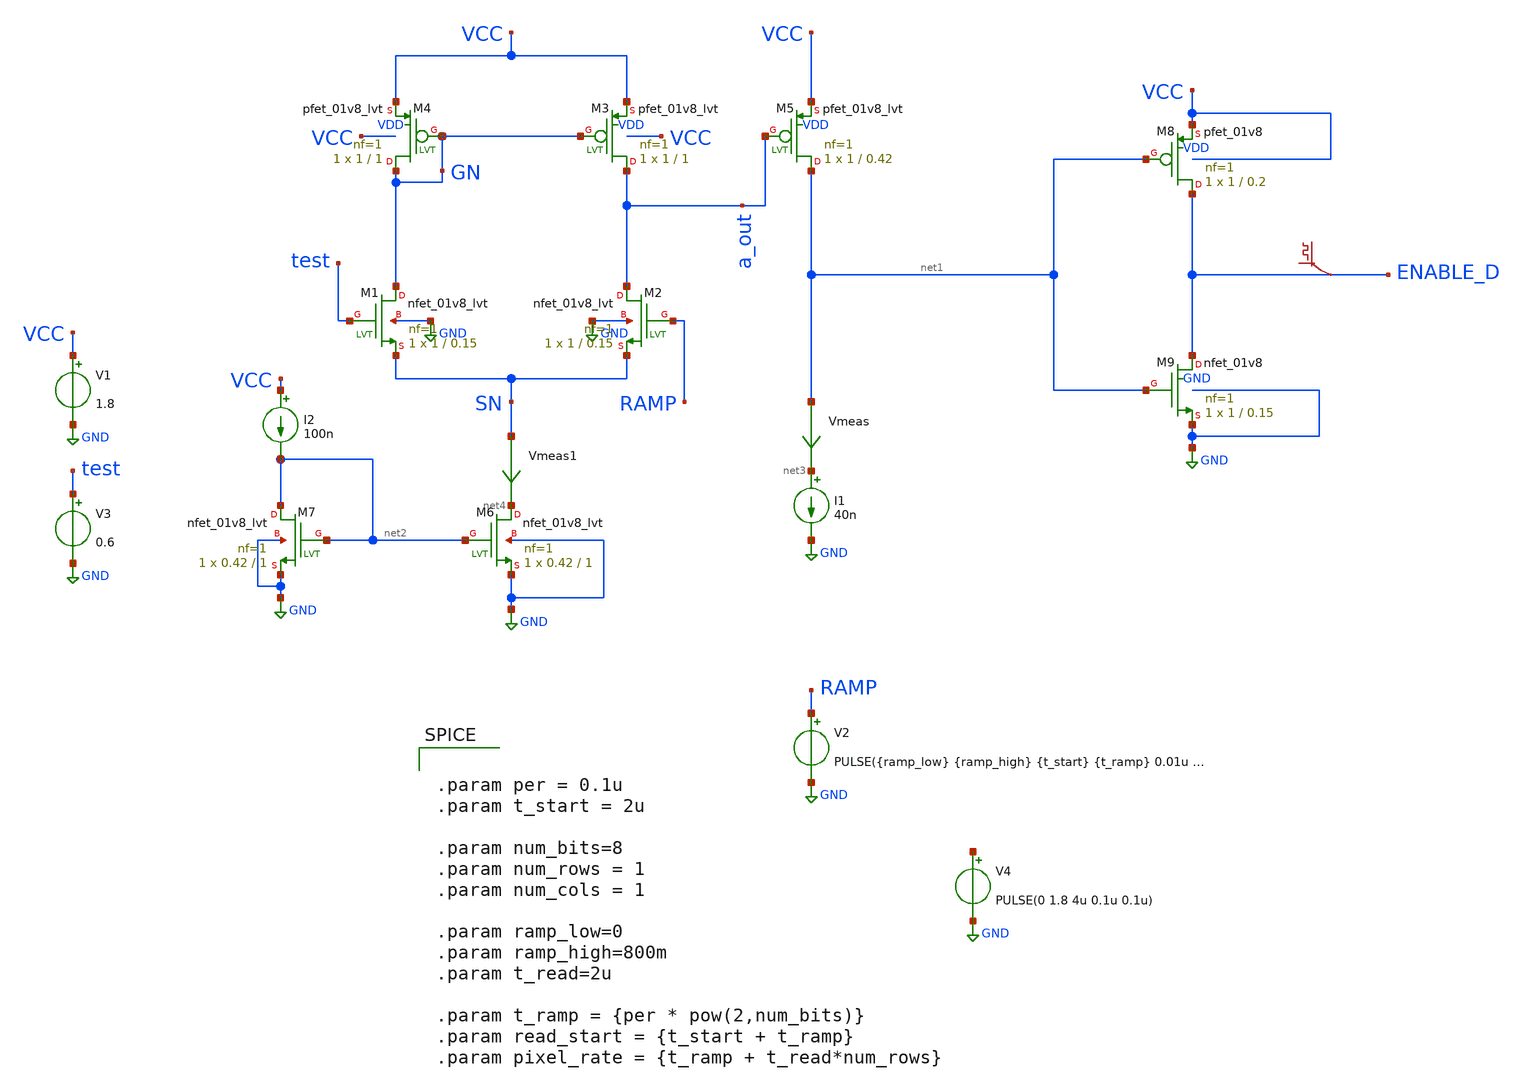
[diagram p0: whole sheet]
** sch_path: xschem/testbench/comp_test.sch
**.subckt comp_test
V1 VCC GND 1.8
V3 test GND 0.6
XM1 GN test SN GND sky130_fd_pr__nfet_01v8_lvt L=0.15 W=1 nf=1 ad='int((nf+1)/2) * W/nf * 0.29' as='int((nf+2)/2) * W/nf * 0.29'
+ pd='2*int((nf+1)/2) * (W/nf + 0.29)' ps='2*int((nf+2)/2) * (W/nf + 0.29)' nrd='0.29 / W' nrs='0.29 / W'
+ sa=0 sb=0 sd=0 mult=1 m=1
XM2 a_out RAMP SN GND sky130_fd_pr__nfet_01v8_lvt L=0.15 W=1 nf=1 ad='int((nf+1)/2) * W/nf * 0.29' as='int((nf+2)/2) * W/nf * 0.29'
+ pd='2*int((nf+1)/2) * (W/nf + 0.29)' ps='2*int((nf+2)/2) * (W/nf + 0.29)' nrd='0.29 / W' nrs='0.29 / W'
+ sa=0 sb=0 sd=0 mult=1 m=1
XM3 a_out GN VCC VDD sky130_fd_pr__pfet_01v8_lvt L=1 W=1 nf=1 ad='int((nf+1)/2) * W/nf * 0.29' as='int((nf+2)/2) * W/nf * 0.29'
+ pd='2*int((nf+1)/2) * (W/nf + 0.29)' ps='2*int((nf+2)/2) * (W/nf + 0.29)' nrd='0.29 / W' nrs='0.29 / W'
+ sa=0 sb=0 sd=0 mult=1 m=1
XM4 GN GN VCC VDD sky130_fd_pr__pfet_01v8_lvt L=1 W=1 nf=1 ad='int((nf+1)/2) * W/nf * 0.29' as='int((nf+2)/2) * W/nf * 0.29'
+ pd='2*int((nf+1)/2) * (W/nf + 0.29)' ps='2*int((nf+2)/2) * (W/nf + 0.29)' nrd='0.29 / W' nrs='0.29 / W'
+ sa=0 sb=0 sd=0 mult=1 m=1
XM5 net1 a_out VCC VDD sky130_fd_pr__pfet_01v8_lvt L=0.42 W=1 nf=1 ad='int((nf+1)/2) * W/nf * 0.29' as='int((nf+2)/2) * W/nf * 0.29'
+ pd='2*int((nf+1)/2) * (W/nf + 0.29)' ps='2*int((nf+2)/2) * (W/nf + 0.29)' nrd='0.29 / W' nrs='0.29 / W'
+ sa=0 sb=0 sd=0 mult=1 m=1
I1 net3 GND 40n
XM8 ENABLE_D net1 VCC VDD sky130_fd_pr__pfet_01v8 L=0.2 W=1 nf=1 ad='int((nf+1)/2) * W/nf * 0.29' as='int((nf+2)/2) * W/nf * 0.29'
+ pd='2*int((nf+1)/2) * (W/nf + 0.29)' ps='2*int((nf+2)/2) * (W/nf + 0.29)' nrd='0.29 / W' nrs='0.29 / W'
+ sa=0 sb=0 sd=0 mult=1 m=1
XM9 ENABLE_D net1 GND GND sky130_fd_pr__nfet_01v8 L=0.15 W=1 nf=1 ad='int((nf+1)/2) * W/nf * 0.29' as='int((nf+2)/2) * W/nf * 0.29'
+ pd='2*int((nf+1)/2) * (W/nf + 0.29)' ps='2*int((nf+2)/2) * (W/nf + 0.29)' nrd='0.29 / W' nrs='0.29 / W'
+ sa=0 sb=0 sd=0 mult=1 m=1
.save v(enable_d)
Vmeas net1 net3 0
.save i(vmeas)
Vmeas1 SN net4 0
.save i(vmeas1)
XM6 net4 net2 GND GND sky130_fd_pr__nfet_01v8_lvt L=1 W=0.42 nf=1 ad='int((nf+1)/2) * W/nf * 0.29' as='int((nf+2)/2) * W/nf * 0.29'
+ pd='2*int((nf+1)/2) * (W/nf + 0.29)' ps='2*int((nf+2)/2) * (W/nf + 0.29)' nrd='0.29 / W' nrs='0.29 / W'
+ sa=0 sb=0 sd=0 mult=1 m=1
XM7 net2 net2 GND GND sky130_fd_pr__nfet_01v8_lvt L=1 W=0.42 nf=1 ad='int((nf+1)/2) * W/nf * 0.29' as='int((nf+2)/2) * W/nf * 0.29'
+ pd='2*int((nf+1)/2) * (W/nf + 0.29)' ps='2*int((nf+2)/2) * (W/nf + 0.29)' nrd='0.29 / W' nrs='0.29 / W'
+ sa=0 sb=0 sd=0 mult=1 m=1
I2 VCC net2 100n
V2 RAMP GND PULSE({ramp_low} {ramp_high} {t_start} {t_ramp} 0.01u {pixel_rate-t_ramp} {pixel_rate})
V4 net5 GND PULSE(0 1.8 4u 0.1u 0.1u)
**** begin user architecture code

** opencircuitdesign pdks install
.lib $::SKYWATER_MODELS/sky130.lib.spice tt




.param per = 0.1u
.param t_start = 2u

.param num_bits=8
.param num_rows = 1
.param num_cols = 1

.param ramp_low=0
.param ramp_high=800m
.param t_read=2u

.param t_ramp = {per * pow(2,num_bits)}
.param read_start = {t_start + t_ramp}
.param pixel_rate = {t_ramp + t_read*num_rows}


**** end user architecture code
**.ends
.GLOBAL GND
**** begin user architecture code


.control
save all

*ac dec 10 0.1 1000Meg
*plot vdb(ENABLE_D) xlog


*dc v4 0 0.85 0.0001 v3 0 0.8 0.1
*plot deriv(v(ENABLE_D))
tran 0.01u 25u

plot v(SN) v(RAMP) v(test)
plot i(vmeas1)
write test.txt out
.endc


**** end user architecture code
.end
